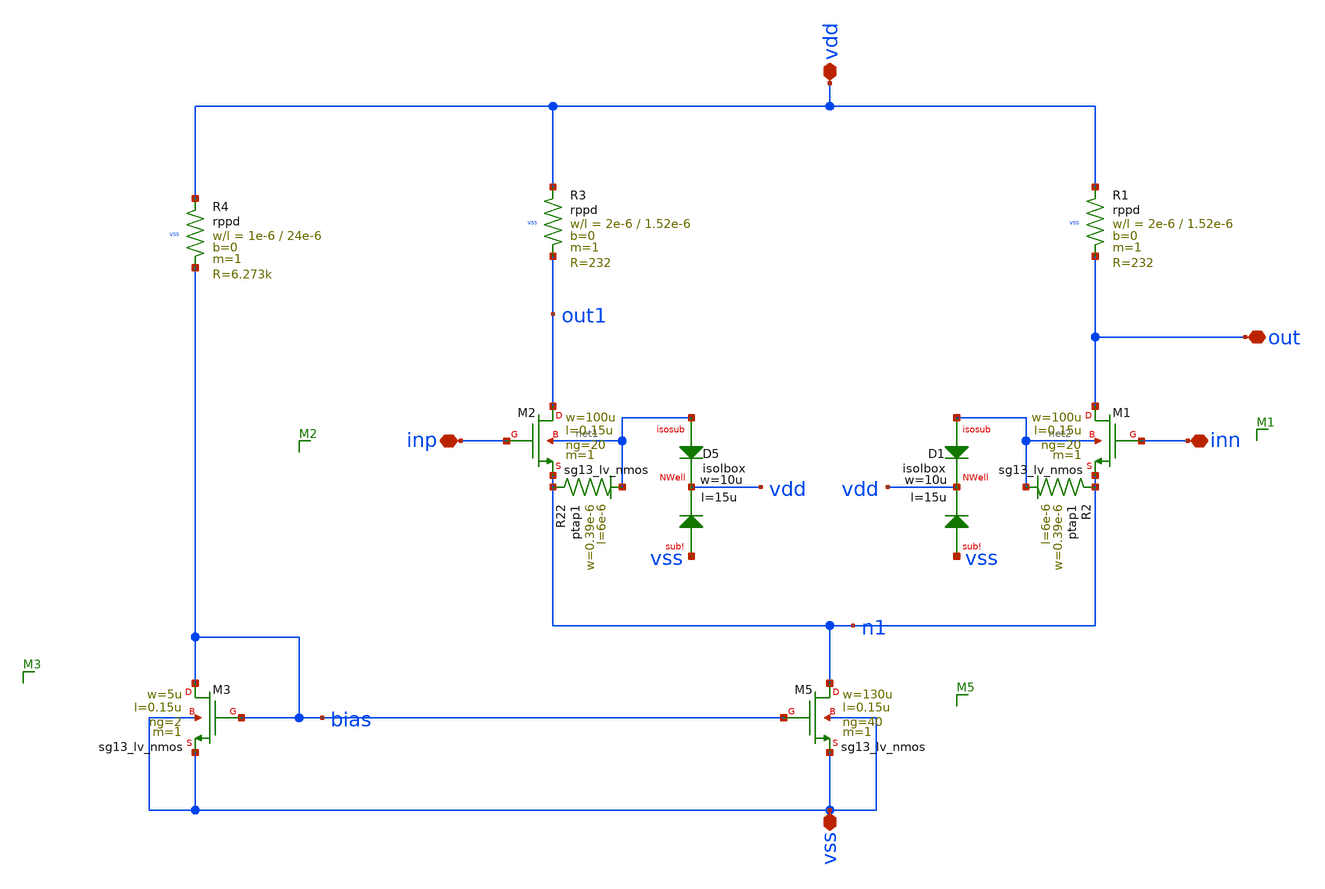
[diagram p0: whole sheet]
** sch_path: LNA7096-main/schematic/xschem/05a_d2s/d2s.sch
**.subckt d2s vdd vss out inp inn
*.iopin vdd
*.iopin vss
*.iopin out
*.iopin inp
*.iopin inn
XR3 vdd out1 vss rppd w=2e-6 l=1.52e-6 m=1 b=0 mm_ok=1
XR1 vdd out vss rppd w=2e-6 l=1.52e-6 m=1 b=0 mm_ok=1
XM2 out1 inp n1 net1 sg13_lv_nmos w=100u l=0.15u ng=20 m=1 mm_ok=1
XD5 net1 vdd vss isolbox l=15u w=10u
XR22 n1 net1 ptap1 R=64.81 w=0.39e-6 l=6e-6
XM5 n1 bias vss vss sg13_lv_nmos w=130u l=0.15u ng=40 m=1 mm_ok=1
XM1 out inn n1 net2 sg13_lv_nmos w=100u l=0.15u ng=20 m=1 mm_ok=1
XD1 net2 vdd vss isolbox l=15u w=10u
XR2 n1 net2 ptap1 R=64.81 w=0.39e-6 l=6e-6
XM3 bias bias vss vss sg13_lv_nmos w=5u l=0.15u ng=2 m=1 mm_ok=1
XR4 vdd bias vss rppd w=1e-6 l=24e-6 m=1 b=0 mm_ok=1
**.ends
.end
